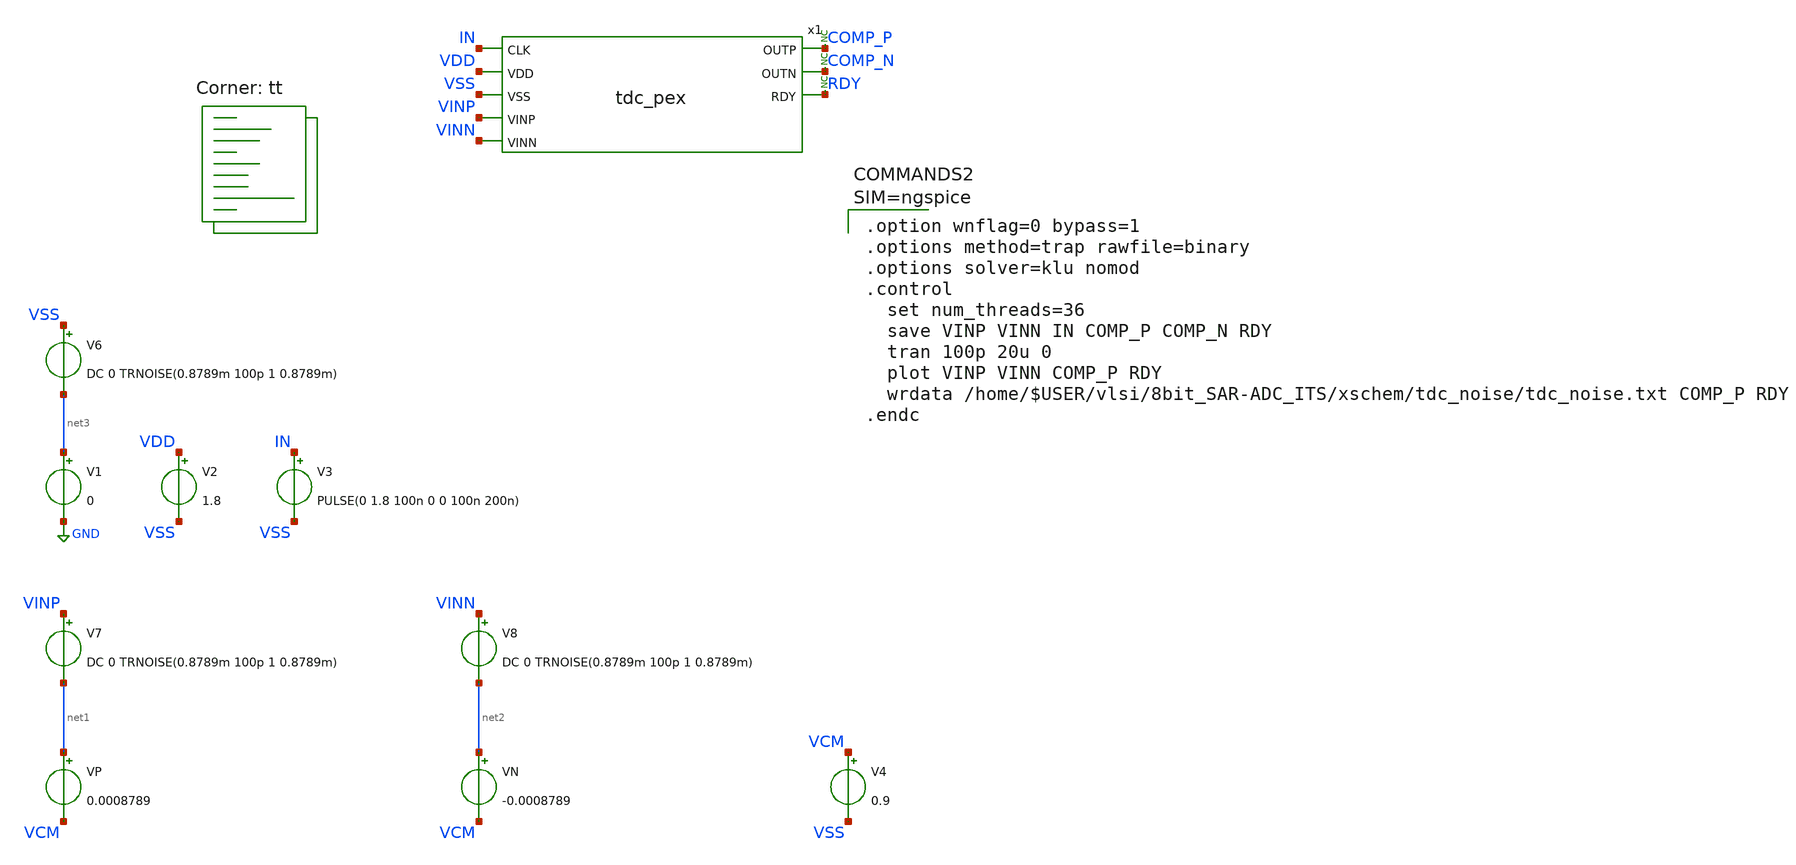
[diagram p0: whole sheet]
** sch_path: xschem/tdc_tb_noise.sch
**.subckt tdc_tb_noise
V1 net3 GND 0
V2 VDD VSS 1.8
V4 VCM VSS 0.9
x1 IN VDD VSS VINP VINN COMP_P COMP_N RDY tdc_pex
* noconn COMP_P
* noconn COMP_N
* noconn RDY
V3 IN VSS PULSE(0 1.8 100n 0 0 100n 200n)
V7 VINP net1 DC 0 TRNOISE(0.8789m 100p 1 0.8789m)
V8 VINN net2 DC 0 TRNOISE(0.8789m 100p 1 0.8789m)
VP net1 VCM 0.0008789
VN net2 VCM -0.0008789
V6 VSS net3 DC 0 TRNOISE(0.8789m 100p 1 0.8789m)
**** begin user architecture code
.lib $::SKYWATER_MODELS/sky130.lib.spice tt


.option wnflag=0 bypass=1
.options method=trap rawfile=binary
.options solver=klu nomod
.control
  set num_threads=36
  save VINP VINN IN COMP_P COMP_N RDY
  tran 100p 20u 0
  plot VINP VINN COMP_P RDY
  wrdata /home/$USER/vlsi/8bit_SAR-ADC_ITS/xschem/tdc_noise/tdc_noise.txt COMP_P RDY
.endc




** opencircuitdesign pdks install
* .lib $::SKYWATER_MODELS/sky130.lib.spice tt
*.include $PDK_ROOT/$PDK/libs.ref/sky130_fd_sc_hdll/spice/sky130_fd_sc_hdll.spice
.include $PDK_ROOT/$PDK/libs.ref/sky130_fd_sc_hs/spice/sky130_fd_sc_hs.spice
.include $PDK_ROOT/$PDK/libs.ref/sky130_fd_sc_hd/spice/sky130_fd_sc_hd.spice

**** end user architecture code
**.ends

* expanding   symbol:  tdc_pex.sym # of pins=8
** sym_path: xschem/tdc_pex.sym
.include /home/mthudaa/vlsi/8bit_SAR-ADC_ITS/xschem/tdc_pex.spice
.GLOBAL GND
.end
